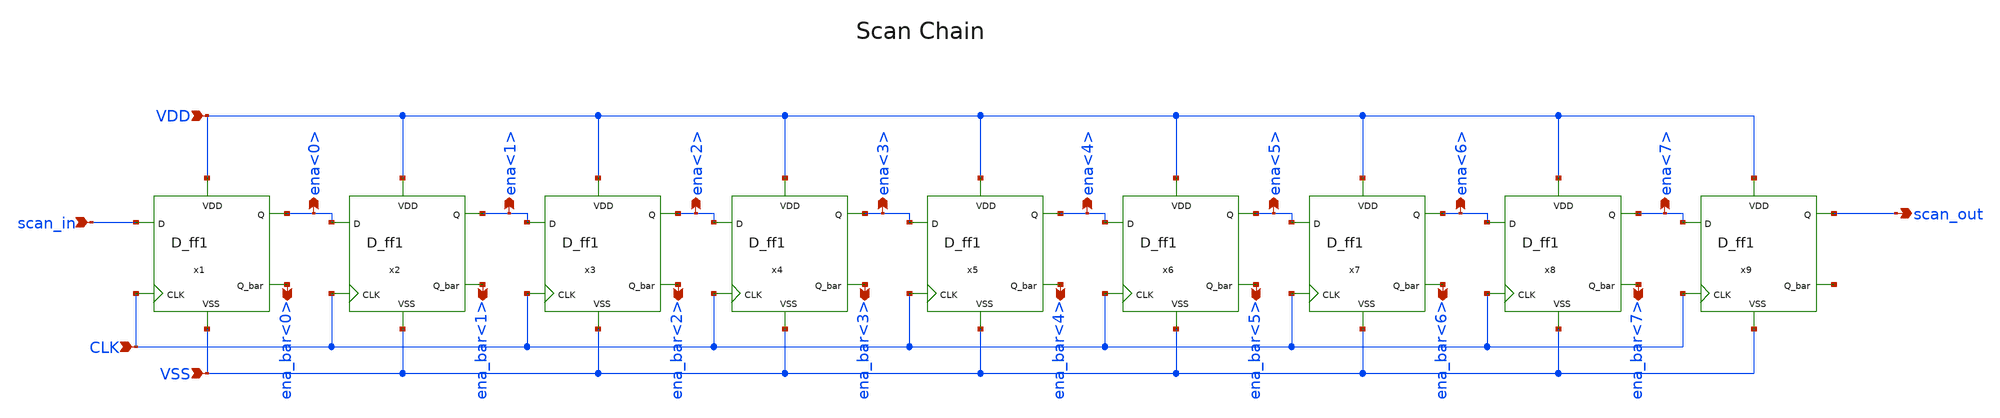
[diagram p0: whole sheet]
** sch_path: designs/libs/core_digital/schem/scan_chain.sch
**.subckt scan_chain scan_in CLK VSS VDD ena_bar<0> ena_bar<2> ena_bar<1> ena_bar<3> ena_bar<4>
*+ ena_bar<5> ena_bar<6> ena_bar<7> scan_out ena<7> ena<6> ena<5> ena<4> ena<3> ena<2> ena<1> ena<0>
*.ipin scan_in
*.ipin CLK
*.ipin VSS
*.ipin VDD
*.opin ena_bar<0>
*.opin ena_bar<2>
*.opin ena_bar<1>
*.opin ena_bar<3>
*.opin ena_bar<4>
*.opin ena_bar<5>
*.opin ena_bar<6>
*.opin ena_bar<7>
*.opin scan_out
*.opin ena<7>
*.opin ena<6>
*.opin ena<5>
*.opin ena<4>
*.opin ena<3>
*.opin ena<2>
*.opin ena<1>
*.opin ena<0>
x1 VDD scan_in ena<0> ena_bar<0> CLK VSS D_ff1
x2 VDD ena<0> ena<1> ena_bar<1> CLK VSS D_ff1
x3 VDD ena<1> ena<2> ena_bar<2> CLK VSS D_ff1
x4 VDD ena<2> ena<3> ena_bar<3> CLK VSS D_ff1
x5 VDD ena<3> ena<4> ena_bar<4> CLK VSS D_ff1
x6 VDD ena<4> ena<5> ena_bar<5> CLK VSS D_ff1
x7 VDD ena<5> ena<6> ena_bar<6> CLK VSS D_ff1
x8 VDD ena<6> ena<7> ena_bar<7> CLK VSS D_ff1
x9 VDD ena<7> scan_out net1 CLK VSS D_ff1
**.ends
.end
